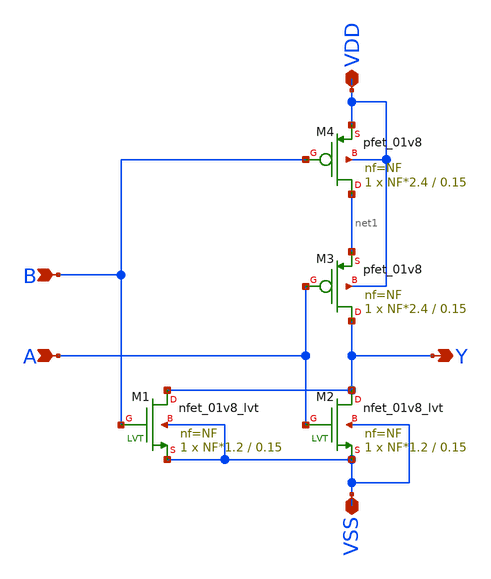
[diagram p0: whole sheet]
** sch_path: xschem_lib/DFFRAM_full_custom/nor.sch
**.subckt nor VDD VSS Y A B
*.iopin VDD
*.iopin VSS
*.opin Y
*.ipin A
*.ipin B
XM1 Y B VSS VSS sky130_fd_pr__nfet_01v8_lvt L=0.15 W=NF*1.2 nf=NF ad='int((nf+1)/2) * W/nf * 0.29' as='int((nf+2)/2) * W/nf * 0.29'
+ pd='2*int((nf+1)/2) * (W/nf + 0.29)' ps='2*int((nf+2)/2) * (W/nf + 0.29)' nrd='0.29 / W' nrs='0.29 / W'
+ sa=0 sb=0 sd=0 mult=1 m=1
XM4 net1 B VDD VDD sky130_fd_pr__pfet_01v8 L=0.15 W=NF*2.4 nf=NF ad='int((nf+1)/2) * W/nf * 0.29' as='int((nf+2)/2) * W/nf * 0.29'
+ pd='2*int((nf+1)/2) * (W/nf + 0.29)' ps='2*int((nf+2)/2) * (W/nf + 0.29)' nrd='0.29 / W' nrs='0.29 / W'
+ sa=0 sb=0 sd=0 mult=1 m=1
XM3 Y A net1 VDD sky130_fd_pr__pfet_01v8 L=0.15 W=NF*2.4 nf=NF ad='int((nf+1)/2) * W/nf * 0.29' as='int((nf+2)/2) * W/nf * 0.29'
+ pd='2*int((nf+1)/2) * (W/nf + 0.29)' ps='2*int((nf+2)/2) * (W/nf + 0.29)' nrd='0.29 / W' nrs='0.29 / W'
+ sa=0 sb=0 sd=0 mult=1 m=1
XM2 Y A VSS VSS sky130_fd_pr__nfet_01v8_lvt L=0.15 W=NF*1.2 nf=NF ad='int((nf+1)/2) * W/nf * 0.29' as='int((nf+2)/2) * W/nf * 0.29'
+ pd='2*int((nf+1)/2) * (W/nf + 0.29)' ps='2*int((nf+2)/2) * (W/nf + 0.29)' nrd='0.29 / W' nrs='0.29 / W'
+ sa=0 sb=0 sd=0 mult=1 m=1
**.ends
.end
